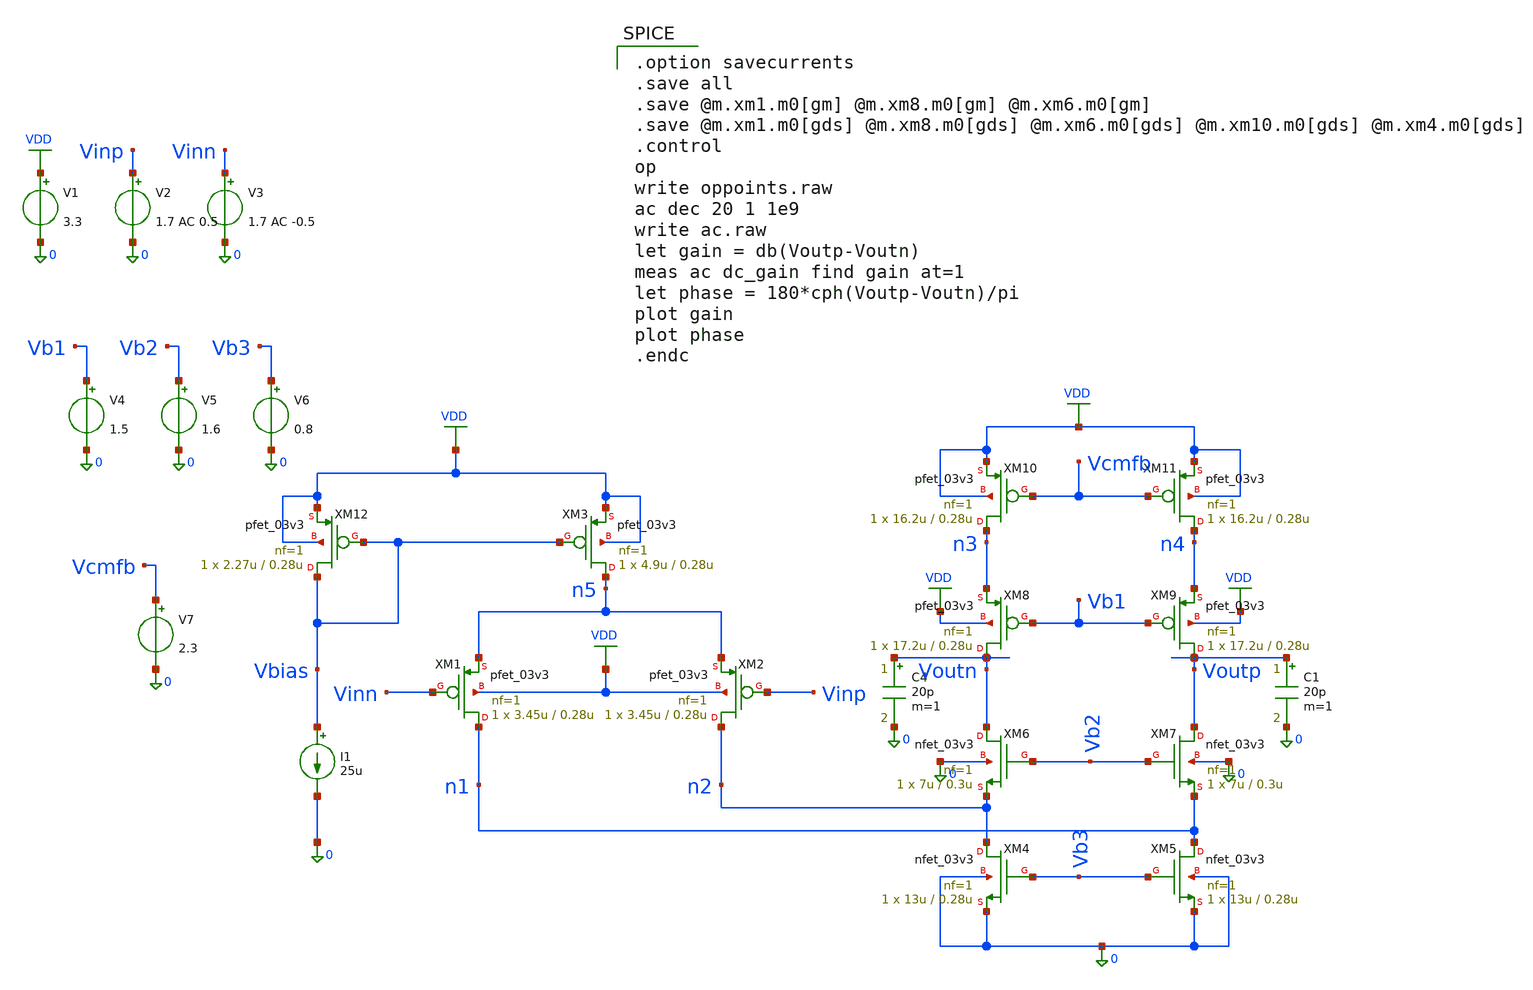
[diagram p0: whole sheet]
** sch_path: ps-filters/foldedcasc.sch
**.subckt foldedcasc
XM4 n2 Vb3 0 0 nfet_03v3 L=0.28u W=13u nf=1 ad='int((nf+1)/2) * W/nf * 0.18u' as='int((nf+2)/2) * W/nf * 0.18u'
+ pd='2*int((nf+1)/2) * (W/nf + 0.18u)' ps='2*int((nf+2)/2) * (W/nf + 0.18u)' nrd='0.18u / W' nrs='0.18u / W'
+ sa=0 sb=0 sd=0 m=1
XM5 n1 Vb3 0 0 nfet_03v3 L=0.28u W=13u nf=1 ad='int((nf+1)/2) * W/nf * 0.18u' as='int((nf+2)/2) * W/nf * 0.18u'
+ pd='2*int((nf+1)/2) * (W/nf + 0.18u)' ps='2*int((nf+2)/2) * (W/nf + 0.18u)' nrd='0.18u / W' nrs='0.18u / W'
+ sa=0 sb=0 sd=0 m=1
XM6 Voutn Vb2 n2 0 nfet_03v3 L=0.3u W=7u nf=1 ad='int((nf+1)/2) * W/nf * 0.18u' as='int((nf+2)/2) * W/nf * 0.18u'
+ pd='2*int((nf+1)/2) * (W/nf + 0.18u)' ps='2*int((nf+2)/2) * (W/nf + 0.18u)' nrd='0.18u / W' nrs='0.18u / W'
+ sa=0 sb=0 sd=0 m=1
XM7 Voutp Vb2 n1 0 nfet_03v3 L=0.3u W=7u nf=1 ad='int((nf+1)/2) * W/nf * 0.18u' as='int((nf+2)/2) * W/nf * 0.18u'
+ pd='2*int((nf+1)/2) * (W/nf + 0.18u)' ps='2*int((nf+2)/2) * (W/nf + 0.18u)' nrd='0.18u / W' nrs='0.18u / W'
+ sa=0 sb=0 sd=0 m=1
XM8 Voutn Vb1 n3 VDD pfet_03v3 L=0.28u W=17.2u nf=1 ad='int((nf+1)/2) * W/nf * 0.18u' as='int((nf+2)/2) * W/nf * 0.18u'
+ pd='2*int((nf+1)/2) * (W/nf + 0.18u)' ps='2*int((nf+2)/2) * (W/nf + 0.18u)' nrd='0.18u / W' nrs='0.18u / W'
+ sa=0 sb=0 sd=0 m=1
XM9 Voutp Vb1 n4 VDD pfet_03v3 L=0.28u W=17.2u nf=1 ad='int((nf+1)/2) * W/nf * 0.18u' as='int((nf+2)/2) * W/nf * 0.18u'
+ pd='2*int((nf+1)/2) * (W/nf + 0.18u)' ps='2*int((nf+2)/2) * (W/nf + 0.18u)' nrd='0.18u / W' nrs='0.18u / W'
+ sa=0 sb=0 sd=0 m=1
XM10 n3 Vcmfb VDD VDD pfet_03v3 L=0.28u W=16.2u nf=1 ad='int((nf+1)/2) * W/nf * 0.18u' as='int((nf+2)/2) * W/nf * 0.18u'
+ pd='2*int((nf+1)/2) * (W/nf + 0.18u)' ps='2*int((nf+2)/2) * (W/nf + 0.18u)' nrd='0.18u / W' nrs='0.18u / W'
+ sa=0 sb=0 sd=0 m=1
XM11 n4 Vcmfb VDD VDD pfet_03v3 L=0.28u W=16.2u nf=1 ad='int((nf+1)/2) * W/nf * 0.18u' as='int((nf+2)/2) * W/nf * 0.18u'
+ pd='2*int((nf+1)/2) * (W/nf + 0.18u)' ps='2*int((nf+2)/2) * (W/nf + 0.18u)' nrd='0.18u / W' nrs='0.18u / W'
+ sa=0 sb=0 sd=0 m=1
V1 VDD 0 3.3
V2 Vinp 0 1.7 AC 0.5
C4 Voutn 0 20p m=1
C1 Voutp 0 20p m=1
V3 Vinn 0 1.7 AC -0.5
I1 Vbias 0 25u
V4 Vb1 0 1.5
V5 Vb2 0 1.6
V6 Vb3 0 0.8
V7 Vcmfb 0 2.3
XM1 n1 Vinn n5 VDD pfet_03v3 L=0.28u W=3.45u nf=1 ad='int((nf+1)/2) * W/nf * 0.18u' as='int((nf+2)/2) * W/nf * 0.18u'
+ pd='2*int((nf+1)/2) * (W/nf + 0.18u)' ps='2*int((nf+2)/2) * (W/nf + 0.18u)' nrd='0.18u / W' nrs='0.18u / W'
+ sa=0 sb=0 sd=0 m=1
XM2 n2 Vinp n5 VDD pfet_03v3 L=0.28u W=3.45u nf=1 ad='int((nf+1)/2) * W/nf * 0.18u' as='int((nf+2)/2) * W/nf * 0.18u'
+ pd='2*int((nf+1)/2) * (W/nf + 0.18u)' ps='2*int((nf+2)/2) * (W/nf + 0.18u)' nrd='0.18u / W' nrs='0.18u / W'
+ sa=0 sb=0 sd=0 m=1
XM3 n5 Vbias VDD VDD pfet_03v3 L=0.28u W=4.9u nf=1 ad='int((nf+1)/2) * W/nf * 0.18u' as='int((nf+2)/2) * W/nf * 0.18u'
+ pd='2*int((nf+1)/2) * (W/nf + 0.18u)' ps='2*int((nf+2)/2) * (W/nf + 0.18u)' nrd='0.18u / W' nrs='0.18u / W'
+ sa=0 sb=0 sd=0 m=1
XM12 Vbias Vbias VDD VDD pfet_03v3 L=0.28u W=2.27u nf=1 ad='int((nf+1)/2) * W/nf * 0.18u' as='int((nf+2)/2) * W/nf * 0.18u'
+ pd='2*int((nf+1)/2) * (W/nf + 0.18u)' ps='2*int((nf+2)/2) * (W/nf + 0.18u)' nrd='0.18u / W' nrs='0.18u / W'
+ sa=0 sb=0 sd=0 m=1
**** begin user architecture code

.include $::180MCU_MODELS/design.ngspice
.lib $::180MCU_MODELS/sm141064.ngspice typical
.lib $::180MCU_MODELS/smbb000149.ngspice typical


.option savecurrents
.save all
.save @m.xm1.m0[gm] @m.xm8.m0[gm] @m.xm6.m0[gm]
.save @m.xm1.m0[gds] @m.xm8.m0[gds] @m.xm6.m0[gds] @m.xm10.m0[gds] @m.xm4.m0[gds]
.control
op
write oppoints.raw
ac dec 20 1 1e9
write ac.raw
let gain = db(Voutp-Voutn)
meas ac dc_gain find gain at=1
let phase = 180*cph(Voutp-Voutn)/pi
plot gain
plot phase
.endc

**** end user architecture code
**.ends
.GLOBAL VDD
.end
